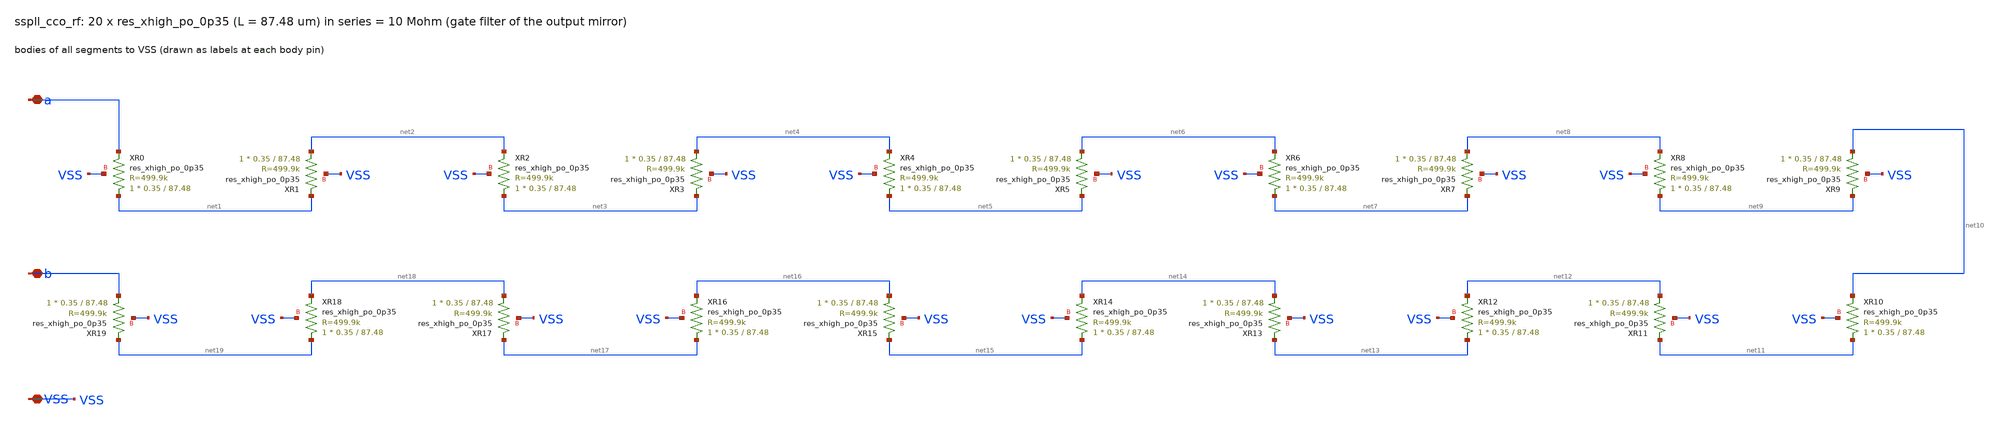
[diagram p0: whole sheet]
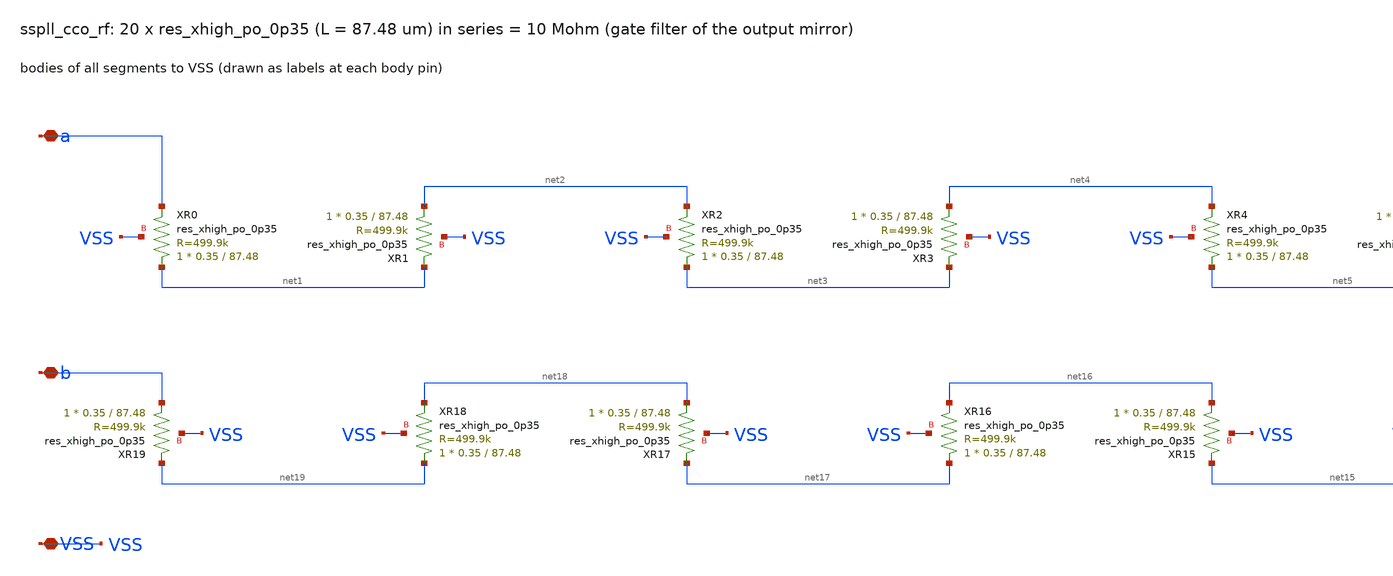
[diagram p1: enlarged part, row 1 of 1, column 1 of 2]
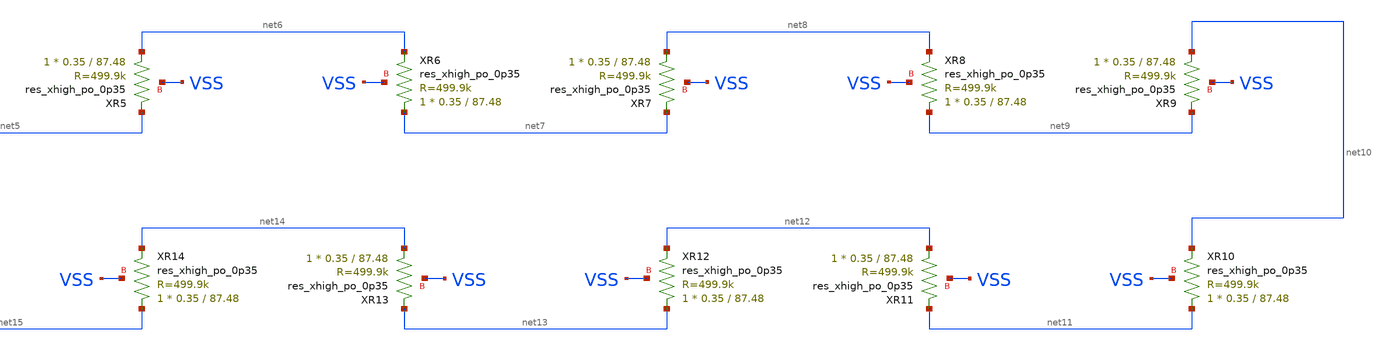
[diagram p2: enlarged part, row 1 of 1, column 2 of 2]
** sch_path: xschem/cco/sspll_cco_rf.sch
**.subckt sspll_cco_rf a b VSS
*.iopin a
*.iopin b
*.iopin VSS
XXR0 net1 a VSS sky130_fd_pr__res_xhigh_po_0p35 L=87.48 mult=1 m=1
XXR1 net2 net1 VSS sky130_fd_pr__res_xhigh_po_0p35 L=87.48 mult=1 m=1
XXR2 net3 net2 VSS sky130_fd_pr__res_xhigh_po_0p35 L=87.48 mult=1 m=1
XXR3 net4 net3 VSS sky130_fd_pr__res_xhigh_po_0p35 L=87.48 mult=1 m=1
XXR4 net5 net4 VSS sky130_fd_pr__res_xhigh_po_0p35 L=87.48 mult=1 m=1
XXR5 net6 net5 VSS sky130_fd_pr__res_xhigh_po_0p35 L=87.48 mult=1 m=1
XXR6 net7 net6 VSS sky130_fd_pr__res_xhigh_po_0p35 L=87.48 mult=1 m=1
XXR7 net8 net7 VSS sky130_fd_pr__res_xhigh_po_0p35 L=87.48 mult=1 m=1
XXR8 net9 net8 VSS sky130_fd_pr__res_xhigh_po_0p35 L=87.48 mult=1 m=1
XXR9 net10 net9 VSS sky130_fd_pr__res_xhigh_po_0p35 L=87.48 mult=1 m=1
XXR10 net11 net10 VSS sky130_fd_pr__res_xhigh_po_0p35 L=87.48 mult=1 m=1
XXR11 net12 net11 VSS sky130_fd_pr__res_xhigh_po_0p35 L=87.48 mult=1 m=1
XXR12 net13 net12 VSS sky130_fd_pr__res_xhigh_po_0p35 L=87.48 mult=1 m=1
XXR13 net14 net13 VSS sky130_fd_pr__res_xhigh_po_0p35 L=87.48 mult=1 m=1
XXR14 net15 net14 VSS sky130_fd_pr__res_xhigh_po_0p35 L=87.48 mult=1 m=1
XXR15 net16 net15 VSS sky130_fd_pr__res_xhigh_po_0p35 L=87.48 mult=1 m=1
XXR16 net17 net16 VSS sky130_fd_pr__res_xhigh_po_0p35 L=87.48 mult=1 m=1
XXR17 net18 net17 VSS sky130_fd_pr__res_xhigh_po_0p35 L=87.48 mult=1 m=1
XXR18 net19 net18 VSS sky130_fd_pr__res_xhigh_po_0p35 L=87.48 mult=1 m=1
XXR19 b net19 VSS sky130_fd_pr__res_xhigh_po_0p35 L=87.48 mult=1 m=1
**.ends
.end
